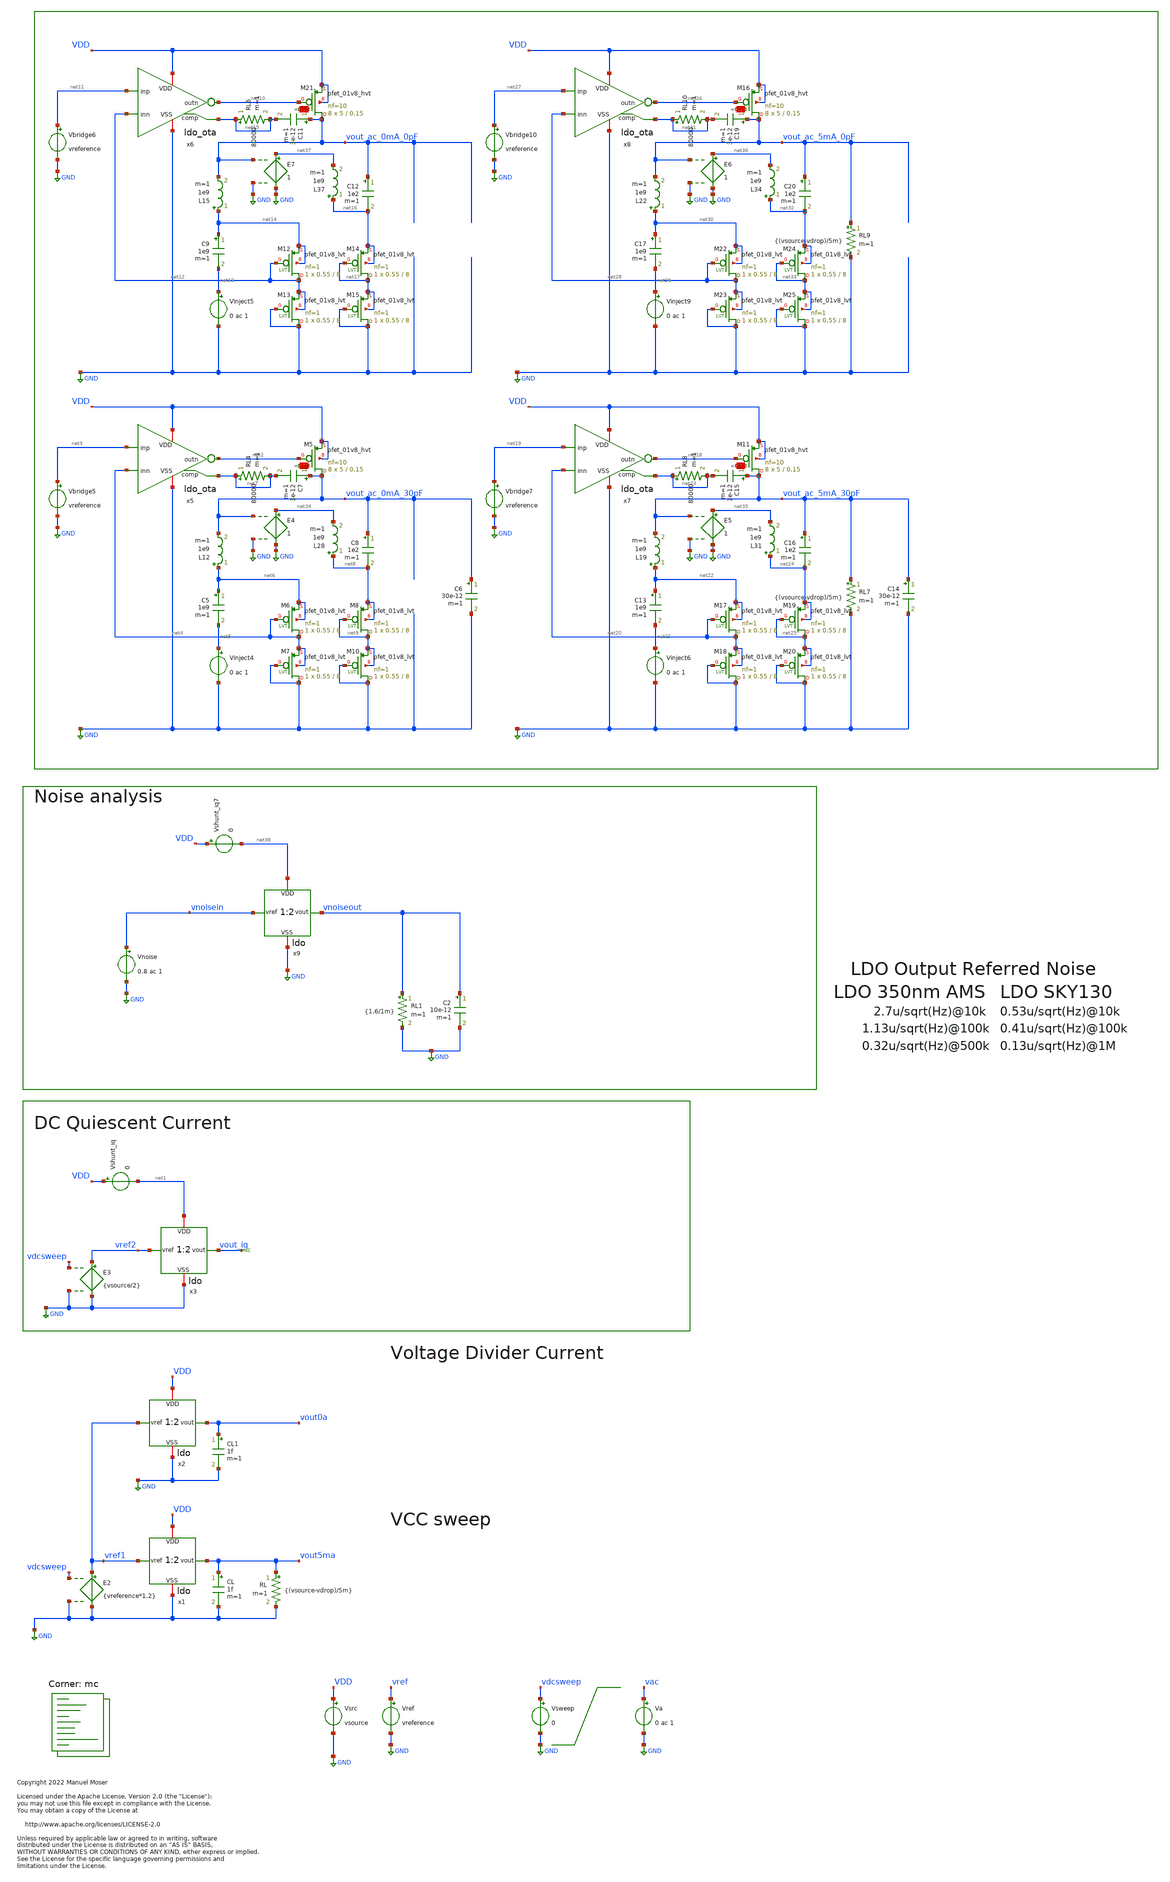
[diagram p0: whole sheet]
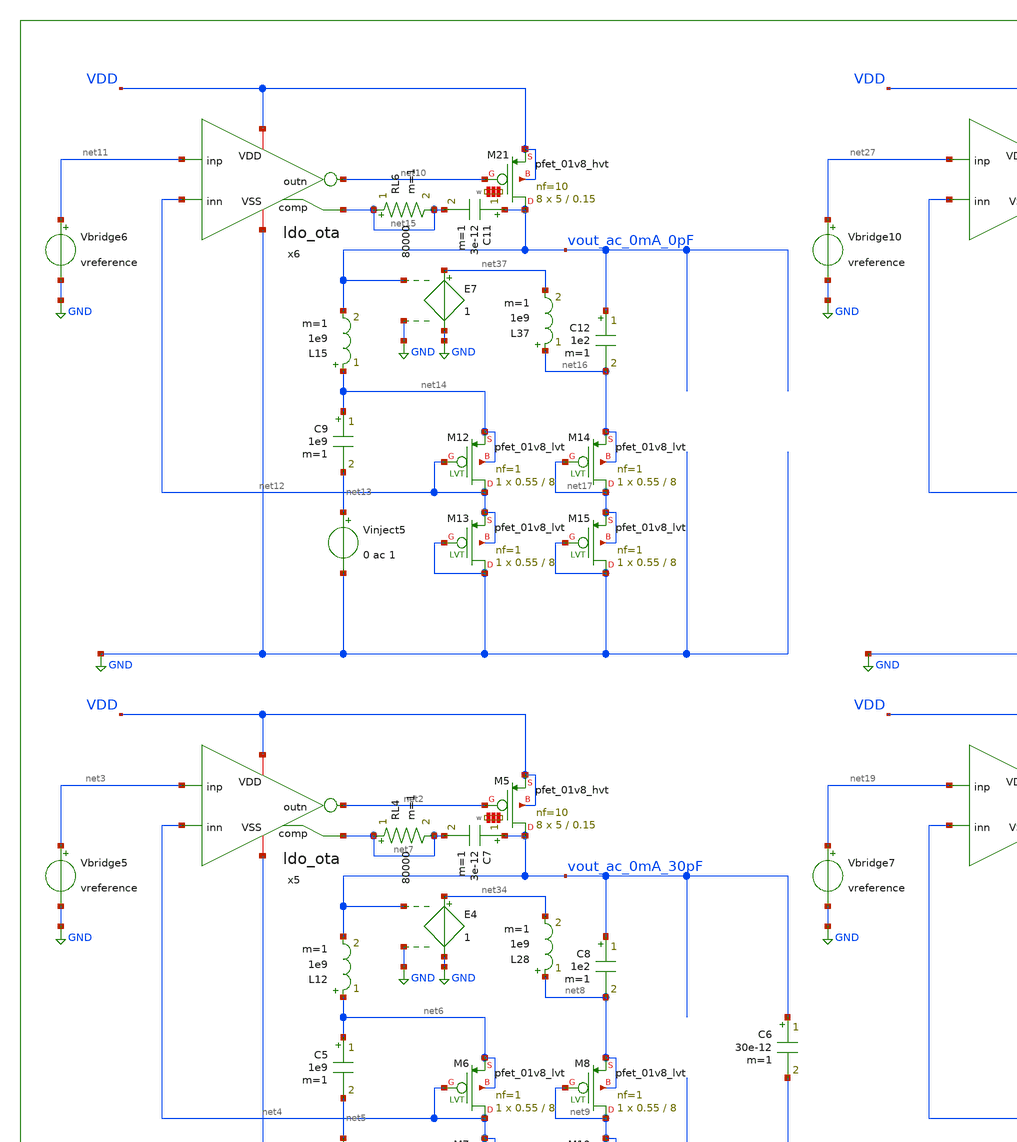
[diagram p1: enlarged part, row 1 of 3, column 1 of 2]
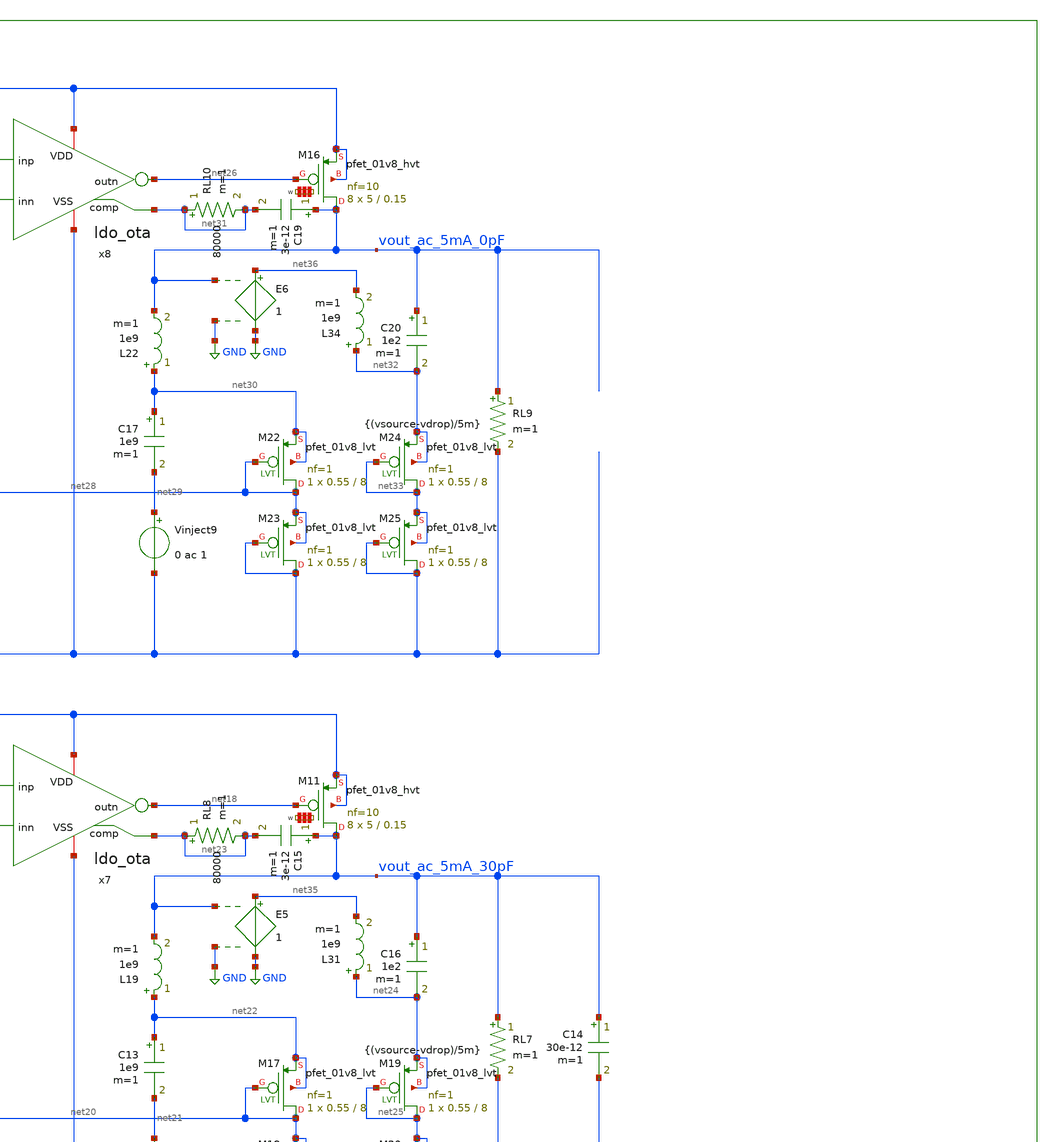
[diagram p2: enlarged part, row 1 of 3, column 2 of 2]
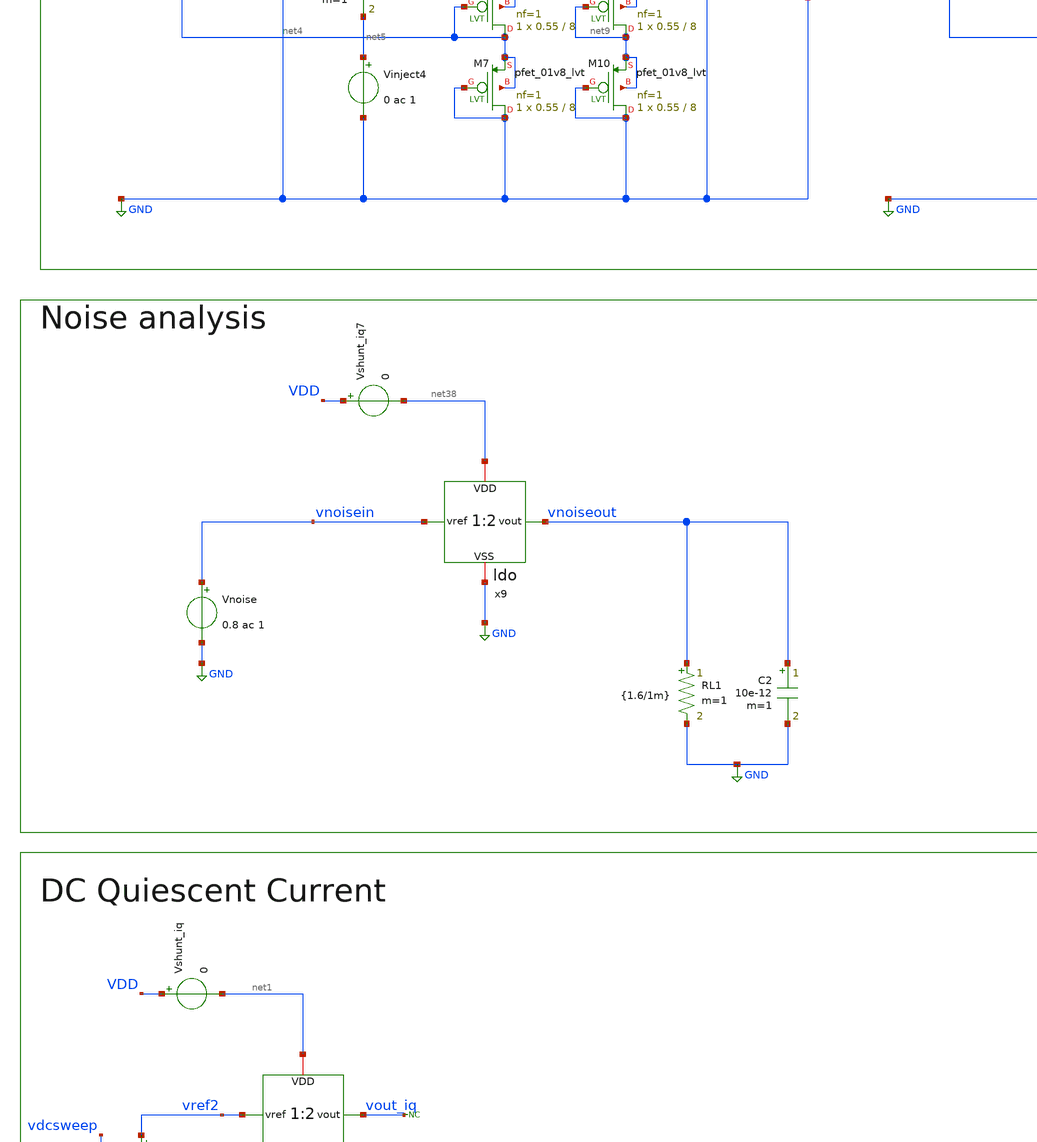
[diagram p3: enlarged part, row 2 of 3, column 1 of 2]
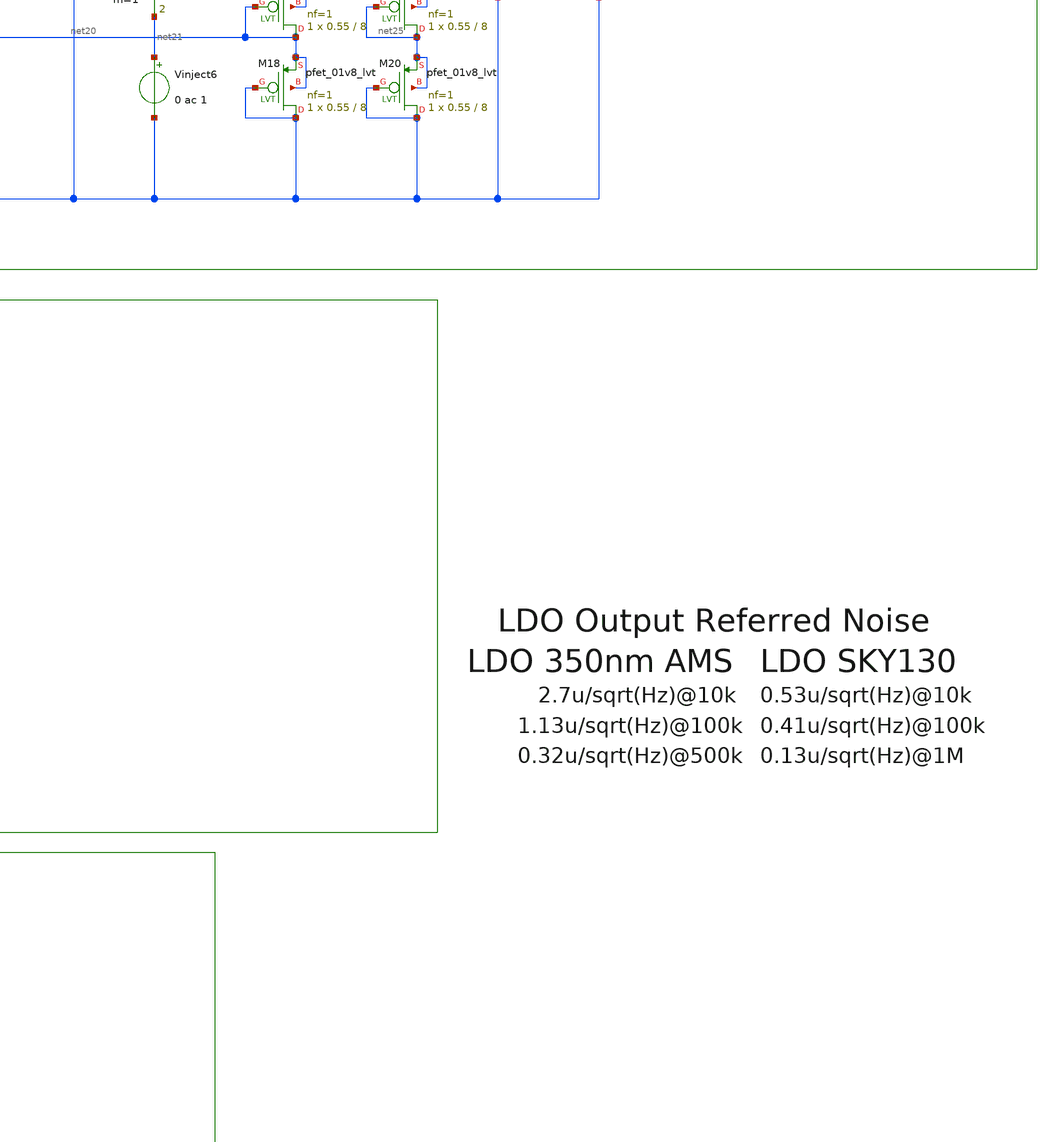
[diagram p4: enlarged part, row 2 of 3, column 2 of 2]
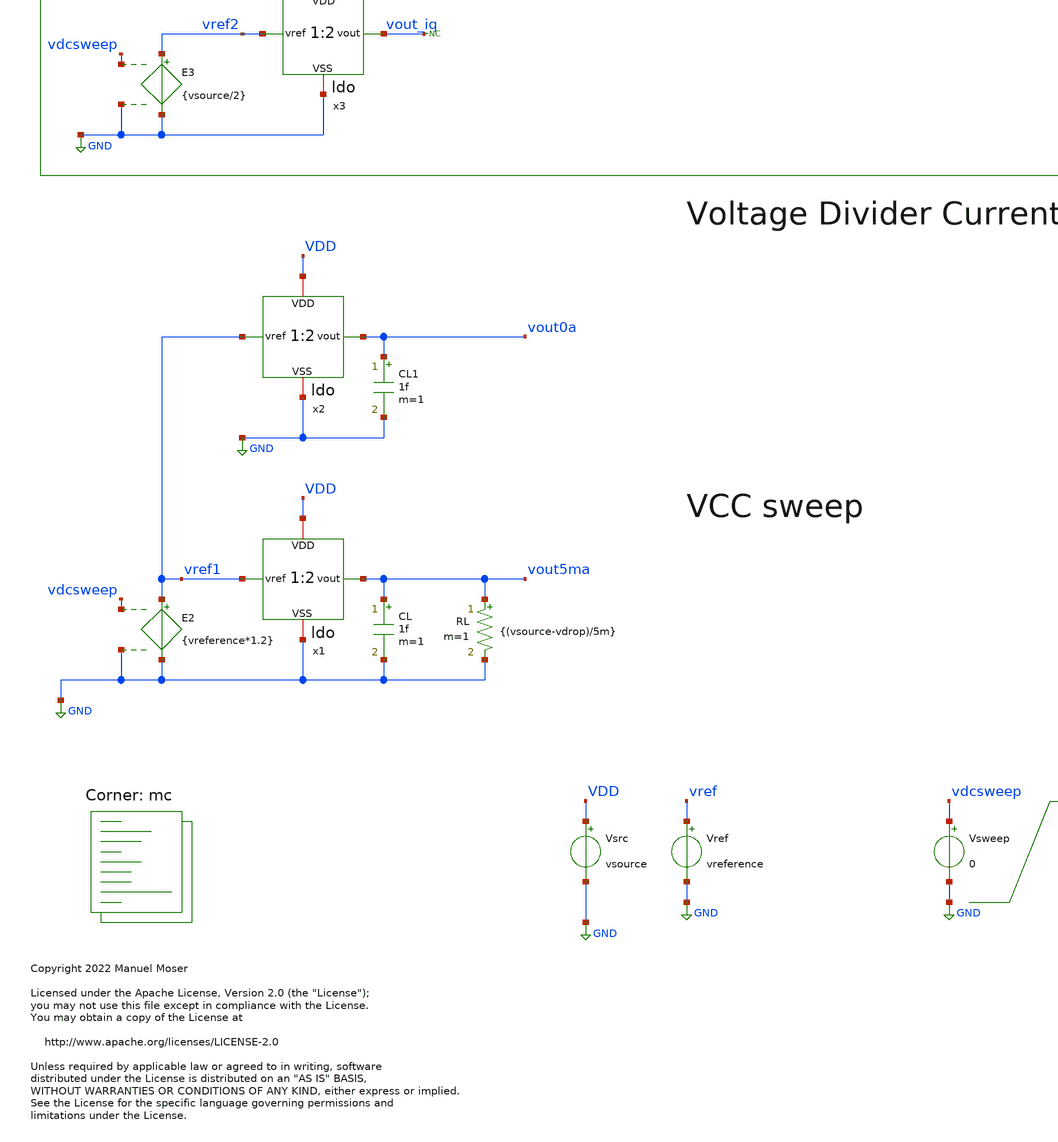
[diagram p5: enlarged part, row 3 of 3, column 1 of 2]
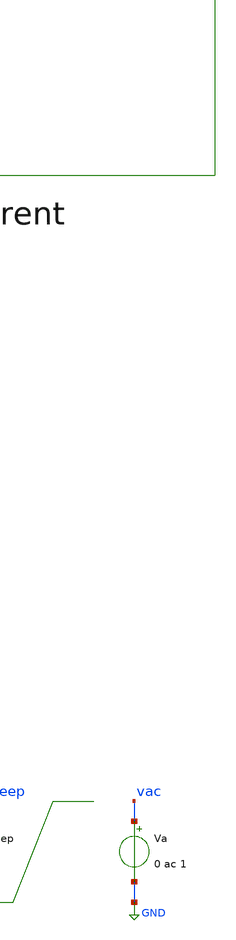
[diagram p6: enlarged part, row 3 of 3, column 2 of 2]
** sch_path: xschem/ldo_tb.sch
* Copyright 2022 Manuel Moser
* Licensed under the Apache License, Version 2.0 (the "License");
**.subckt ldo_tb
Vref vref GND vreference
Vsrc VDD GND vsource
Va vac GND 0 ac 1
CL vout5ma GND 1f m=1
RL vout5ma GND {(vsource-vdrop)/5m} m=1
x1 VDD vref1 vout5ma GND ldo
CL1 vout0a GND 1f m=1
x2 VDD vref1 vout0a GND ldo
Vsweep vdcsweep GND 0
E2 vref1 GND vdcsweep GND {vreference*1.2}
x3 net1 vref2 vout_iq GND ldo
Vshunt_iq VDD net1 0
E3 vref2 GND vdcsweep GND {vsource/2}
* noconn vout_iq
Vnoise vnoisein GND 0.8 ac 1
RL1 vnoiseout GND {1.6/1m} m=1
C2 vnoiseout GND 10e-12 m=1
x5 VDD net3 net2 net4 GND net7 ldo_ota
L12 net6 vout_ac_0mA_30pF 1e9 m=1
C5 net6 net5 1e9 m=1
Vinject4 net5 GND 0 ac 1
Vbridge5 net3 GND vreference
C6 vout_ac_0mA_30pF GND 30e-12 m=1
C7 vout_ac_0mA_30pF net7 3e-12 m=1
RL4 net7 net7 80000 m=1
XM6 net4 net4 net6 net6 sky130_fd_pr__pfet_01v8_lvt L=8 W=0.55 nf=1 ad='int((nf+1)/2) * W/nf * 0.29'
+ as='int((nf+2)/2) * W/nf * 0.29' pd='2*int((nf+1)/2) * (W/nf + 0.29)' ps='2*int((nf+2)/2) * (W/nf + 0.29)'
+ nrd='0.29 / W' nrs='0.29 / W' sa=0 sb=0 sd=0 mult=1 m=1
XM7 GND GND net4 net4 sky130_fd_pr__pfet_01v8_lvt L=8 W=0.55 nf=1 ad='int((nf+1)/2) * W/nf * 0.29' as='int((nf+2)/2) * W/nf * 0.29'
+ pd='2*int((nf+1)/2) * (W/nf + 0.29)' ps='2*int((nf+2)/2) * (W/nf + 0.29)' nrd='0.29 / W' nrs='0.29 / W'
+ sa=0 sb=0 sd=0 mult=1 m=1
XM8 net9 net9 net8 net8 sky130_fd_pr__pfet_01v8_lvt L=8 W=0.55 nf=1 ad='int((nf+1)/2) * W/nf * 0.29'
+ as='int((nf+2)/2) * W/nf * 0.29' pd='2*int((nf+1)/2) * (W/nf + 0.29)' ps='2*int((nf+2)/2) * (W/nf + 0.29)'
+ nrd='0.29 / W' nrs='0.29 / W' sa=0 sb=0 sd=0 mult=1 m=1
XM10 GND GND net9 net9 sky130_fd_pr__pfet_01v8_lvt L=8 W=0.55 nf=1 ad='int((nf+1)/2) * W/nf * 0.29' as='int((nf+2)/2) * W/nf * 0.29'
+ pd='2*int((nf+1)/2) * (W/nf + 0.29)' ps='2*int((nf+2)/2) * (W/nf + 0.29)' nrd='0.29 / W' nrs='0.29 / W'
+ sa=0 sb=0 sd=0 mult=1 m=1
C8 vout_ac_0mA_30pF net8 1e2 m=1
x6 VDD net11 net10 net12 GND net15 ldo_ota
L15 net14 vout_ac_0mA_0pF 1e9 m=1
C9 net14 net13 1e9 m=1
Vinject5 net13 GND 0 ac 1
Vbridge6 net11 GND vreference
C11 vout_ac_0mA_0pF net15 3e-12 m=1
RL6 net15 net15 80000 m=1
XM12 net12 net12 net14 net14 sky130_fd_pr__pfet_01v8_lvt L=8 W=0.55 nf=1 ad='int((nf+1)/2) * W/nf * 0.29'
+ as='int((nf+2)/2) * W/nf * 0.29' pd='2*int((nf+1)/2) * (W/nf + 0.29)' ps='2*int((nf+2)/2) * (W/nf + 0.29)'
+ nrd='0.29 / W' nrs='0.29 / W' sa=0 sb=0 sd=0 mult=1 m=1
XM13 GND GND net12 net12 sky130_fd_pr__pfet_01v8_lvt L=8 W=0.55 nf=1 ad='int((nf+1)/2) * W/nf * 0.29'
+ as='int((nf+2)/2) * W/nf * 0.29' pd='2*int((nf+1)/2) * (W/nf + 0.29)' ps='2*int((nf+2)/2) * (W/nf + 0.29)'
+ nrd='0.29 / W' nrs='0.29 / W' sa=0 sb=0 sd=0 mult=1 m=1
XM14 net17 net17 net16 net16 sky130_fd_pr__pfet_01v8_lvt L=8 W=0.55 nf=1 ad='int((nf+1)/2) * W/nf * 0.29'
+ as='int((nf+2)/2) * W/nf * 0.29' pd='2*int((nf+1)/2) * (W/nf + 0.29)' ps='2*int((nf+2)/2) * (W/nf + 0.29)'
+ nrd='0.29 / W' nrs='0.29 / W' sa=0 sb=0 sd=0 mult=1 m=1
XM15 GND GND net17 net17 sky130_fd_pr__pfet_01v8_lvt L=8 W=0.55 nf=1 ad='int((nf+1)/2) * W/nf * 0.29'
+ as='int((nf+2)/2) * W/nf * 0.29' pd='2*int((nf+1)/2) * (W/nf + 0.29)' ps='2*int((nf+2)/2) * (W/nf + 0.29)'
+ nrd='0.29 / W' nrs='0.29 / W' sa=0 sb=0 sd=0 mult=1 m=1
C12 vout_ac_0mA_0pF net16 1e2 m=1
x7 VDD net19 net18 net20 GND net23 ldo_ota
L19 net22 vout_ac_5mA_30pF 1e9 m=1
C13 net22 net21 1e9 m=1
Vinject6 net21 GND 0 ac 1
Vbridge7 net19 GND vreference
RL7 vout_ac_5mA_30pF GND {(vsource-vdrop)/5m} m=1
C14 vout_ac_5mA_30pF GND 30e-12 m=1
C15 vout_ac_5mA_30pF net23 3e-12 m=1
RL8 net23 net23 80000 m=1
XM17 net20 net20 net22 net22 sky130_fd_pr__pfet_01v8_lvt L=8 W=0.55 nf=1 ad='int((nf+1)/2) * W/nf * 0.29'
+ as='int((nf+2)/2) * W/nf * 0.29' pd='2*int((nf+1)/2) * (W/nf + 0.29)' ps='2*int((nf+2)/2) * (W/nf + 0.29)'
+ nrd='0.29 / W' nrs='0.29 / W' sa=0 sb=0 sd=0 mult=1 m=1
XM18 GND GND net20 net20 sky130_fd_pr__pfet_01v8_lvt L=8 W=0.55 nf=1 ad='int((nf+1)/2) * W/nf * 0.29'
+ as='int((nf+2)/2) * W/nf * 0.29' pd='2*int((nf+1)/2) * (W/nf + 0.29)' ps='2*int((nf+2)/2) * (W/nf + 0.29)'
+ nrd='0.29 / W' nrs='0.29 / W' sa=0 sb=0 sd=0 mult=1 m=1
XM19 net25 net25 net24 net24 sky130_fd_pr__pfet_01v8_lvt L=8 W=0.55 nf=1 ad='int((nf+1)/2) * W/nf * 0.29'
+ as='int((nf+2)/2) * W/nf * 0.29' pd='2*int((nf+1)/2) * (W/nf + 0.29)' ps='2*int((nf+2)/2) * (W/nf + 0.29)'
+ nrd='0.29 / W' nrs='0.29 / W' sa=0 sb=0 sd=0 mult=1 m=1
XM20 GND GND net25 net25 sky130_fd_pr__pfet_01v8_lvt L=8 W=0.55 nf=1 ad='int((nf+1)/2) * W/nf * 0.29'
+ as='int((nf+2)/2) * W/nf * 0.29' pd='2*int((nf+1)/2) * (W/nf + 0.29)' ps='2*int((nf+2)/2) * (W/nf + 0.29)'
+ nrd='0.29 / W' nrs='0.29 / W' sa=0 sb=0 sd=0 mult=1 m=1
C16 vout_ac_5mA_30pF net24 1e2 m=1
x8 VDD net27 net26 net28 GND net31 ldo_ota
L22 net30 vout_ac_5mA_0pF 1e9 m=1
C17 net30 net29 1e9 m=1
Vinject9 net29 GND 0 ac 1
Vbridge10 net27 GND vreference
RL9 vout_ac_5mA_0pF GND {(vsource-vdrop)/5m} m=1
C19 vout_ac_5mA_0pF net31 3e-12 m=1
RL10 net31 net31 80000 m=1
XM22 net28 net28 net30 net30 sky130_fd_pr__pfet_01v8_lvt L=8 W=0.55 nf=1 ad='int((nf+1)/2) * W/nf * 0.29'
+ as='int((nf+2)/2) * W/nf * 0.29' pd='2*int((nf+1)/2) * (W/nf + 0.29)' ps='2*int((nf+2)/2) * (W/nf + 0.29)'
+ nrd='0.29 / W' nrs='0.29 / W' sa=0 sb=0 sd=0 mult=1 m=1
XM23 GND GND net28 net28 sky130_fd_pr__pfet_01v8_lvt L=8 W=0.55 nf=1 ad='int((nf+1)/2) * W/nf * 0.29'
+ as='int((nf+2)/2) * W/nf * 0.29' pd='2*int((nf+1)/2) * (W/nf + 0.29)' ps='2*int((nf+2)/2) * (W/nf + 0.29)'
+ nrd='0.29 / W' nrs='0.29 / W' sa=0 sb=0 sd=0 mult=1 m=1
XM24 net33 net33 net32 net32 sky130_fd_pr__pfet_01v8_lvt L=8 W=0.55 nf=1 ad='int((nf+1)/2) * W/nf * 0.29'
+ as='int((nf+2)/2) * W/nf * 0.29' pd='2*int((nf+1)/2) * (W/nf + 0.29)' ps='2*int((nf+2)/2) * (W/nf + 0.29)'
+ nrd='0.29 / W' nrs='0.29 / W' sa=0 sb=0 sd=0 mult=1 m=1
XM25 GND GND net33 net33 sky130_fd_pr__pfet_01v8_lvt L=8 W=0.55 nf=1 ad='int((nf+1)/2) * W/nf * 0.29'
+ as='int((nf+2)/2) * W/nf * 0.29' pd='2*int((nf+1)/2) * (W/nf + 0.29)' ps='2*int((nf+2)/2) * (W/nf + 0.29)'
+ nrd='0.29 / W' nrs='0.29 / W' sa=0 sb=0 sd=0 mult=1 m=1
C20 vout_ac_5mA_0pF net32 1e2 m=1
L28 net8 net34 1e9 m=1
E4 net34 GND vout_ac_0mA_30pF GND 1
L31 net24 net35 1e9 m=1
E5 net35 GND vout_ac_5mA_30pF GND 1
L34 net32 net36 1e9 m=1
E6 net36 GND vout_ac_5mA_0pF GND 1
L37 net16 net37 1e9 m=1
E7 net37 GND vout_ac_0mA_0pF GND 1
XM5 vout_ac_0mA_30pF net2 VDD VDD sky130_fd_pr__pfet_01v8_hvt L=0.15 W='5 * 10 ' nf=10 ad='int((nf+1)/2) * W / nf * 0.29'
+ as='int((nf+2)/2) * W / nf * 0.29' pd='2*int((nf+1)/2) * (W / nf + 0.29)' ps='2*int((nf+2)/2) * (W / nf + 0.29)'
+ nrd='0.29 / W ' nrs='0.29 / W ' sa=0 sb=0 sd=0 mult=8 m=8
XM11 vout_ac_5mA_30pF net18 VDD VDD sky130_fd_pr__pfet_01v8_hvt L=0.15 W='5 * 10 ' nf=10 ad='int((nf+1)/2) * W / nf * 0.29'
+ as='int((nf+2)/2) * W / nf * 0.29' pd='2*int((nf+1)/2) * (W / nf + 0.29)' ps='2*int((nf+2)/2) * (W / nf + 0.29)'
+ nrd='0.29 / W ' nrs='0.29 / W ' sa=0 sb=0 sd=0 mult=8 m=8
XM16 vout_ac_5mA_0pF net26 VDD VDD sky130_fd_pr__pfet_01v8_hvt L=0.15 W='5 * 10 ' nf=10 ad='int((nf+1)/2) * W / nf * 0.29'
+ as='int((nf+2)/2) * W / nf * 0.29' pd='2*int((nf+1)/2) * (W / nf + 0.29)' ps='2*int((nf+2)/2) * (W / nf + 0.29)'
+ nrd='0.29 / W ' nrs='0.29 / W ' sa=0 sb=0 sd=0 mult=8 m=8
XM21 vout_ac_0mA_0pF net10 VDD VDD sky130_fd_pr__pfet_01v8_hvt L=0.15 W='5 * 10 ' nf=10 ad='int((nf+1)/2) * W / nf * 0.29'
+ as='int((nf+2)/2) * W / nf * 0.29' pd='2*int((nf+1)/2) * (W / nf + 0.29)' ps='2*int((nf+2)/2) * (W / nf + 0.29)'
+ nrd='0.29 / W ' nrs='0.29 / W ' sa=0 sb=0 sd=0 mult=8 m=8
x9 net38 vnoisein vnoiseout GND ldo
Vshunt_iq7 VDD net38 0
**** begin user architecture code



.temp 27
*.option gmin = 1e-16
.option RSHUNT=1E15
.option method = gear

.param vsource = 1.80
.param vdrop = 0.20
.param vreference = {(vsource-vdrop)/2}

.save all
.options savecurrents

.control
set num_threads = 12
write results_ldo.raw
set appendwrite

noise v(vnoiseout) Vnoise dec 10 1 100meg
write results_ldo.raw noise1.all noise2.all

repeat 5
reset

dc vsweep 0 1 0.01 temp -30 60 90
write results_ldo.raw   vref1 vout5ma vout0a x1.vota x1.vfb
+ @m.x1.xm9.msky130_fd_pr__pfet_01v8_lvt[id]  vref2 i(vshunt_iq)

ac dec 10 1 10meg
write results_ldo.raw vout_ac_0mA_0pF vout_ac_0mA_30pF vout_ac_5mA_0pF vout_ac_5mA_30pF

*pz vinject gnd vout_ac_gain gnd vol pz


end

.endc




.lib $::SKYWATER_MODELS/sky130.lib.spice mc
**** end user architecture code
**.ends

* expanding   symbol:  ldo.sym # of pins=4
** sym_path: xschem/ldo.sym
** sch_path: xschem/ldo.sch
.subckt ldo VDD vref vout VSS
*.ipin vref
*.iopin VDD
*.iopin VSS
*.opin vout
x1 VDD vref vota vfb VSS net1 ldo_ota
XM1 vout vota VDD VDD sky130_fd_pr__pfet_01v8 L=0.15 W='5 * 5 ' nf=5 ad='int((nf+1)/2) * W / nf * 0.29'
+ as='int((nf+2)/2) * W / nf * 0.29' pd='2*int((nf+1)/2) * (W / nf + 0.29)' ps='2*int((nf+2)/2) * (W / nf + 0.29)'
+ nrd='0.29 / W ' nrs='0.29 / W ' sa=0 sb=0 sd=0 mult=14 m=14
C1 vout net2 3e-12 m=1
RL2 net1 net2 80000 m=1
XM9 vfb vfb vout vout sky130_fd_pr__pfet_01v8_lvt L=8 W=0.55 nf=1 ad='int((nf+1)/2) * W/nf * 0.29' as='int((nf+2)/2) * W/nf * 0.29'
+ pd='2*int((nf+1)/2) * (W/nf + 0.29)' ps='2*int((nf+2)/2) * (W/nf + 0.29)' nrd='0.29 / W' nrs='0.29 / W'
+ sa=0 sb=0 sd=0 mult=1 m=1
XM3 VSS VSS vfb vfb sky130_fd_pr__pfet_01v8_lvt L=8 W=0.55 nf=1 ad='int((nf+1)/2) * W/nf * 0.29' as='int((nf+2)/2) * W/nf * 0.29'
+ pd='2*int((nf+1)/2) * (W/nf + 0.29)' ps='2*int((nf+2)/2) * (W/nf + 0.29)' nrd='0.29 / W' nrs='0.29 / W'
+ sa=0 sb=0 sd=0 mult=1 m=1
.ends


* expanding   symbol:  ldo_ota.sym # of pins=6
** sym_path: xschem/ldo_ota.sym
** sch_path: xschem/ldo_ota.sch
.subckt ldo_ota VDD inp outn inn VSS comp
*.iopin VDD
*.iopin VSS
*.ipin inp
*.ipin inn
*.opin outn
*.opin comp
x2 bias2 VDD VSS bias1 ldo_isource
XM10 net1 bias2 VDD VDD sky130_fd_pr__pfet_01v8_lvt L=8 W='0.55 * 1 ' nf=1 ad='int((nf+1)/2) * W / nf * 0.29'
+ as='int((nf+2)/2) * W / nf * 0.29' pd='2*int((nf+1)/2) * (W / nf + 0.29)' ps='2*int((nf+2)/2) * (W / nf + 0.29)'
+ nrd='0.29 / W ' nrs='0.29 / W ' sa=0 sb=0 sd=0 mult=1 m=1
XM12 bias2 bias2 net1 VDD sky130_fd_pr__pfet_01v8_lvt L=8 W='0.55 * 4 ' nf=4 ad='int((nf+1)/2) * W / nf * 0.29'
+ as='int((nf+2)/2) * W / nf * 0.29' pd='2*int((nf+1)/2) * (W / nf + 0.29)' ps='2*int((nf+2)/2) * (W / nf + 0.29)'
+ nrd='0.29 / W ' nrs='0.29 / W ' sa=0 sb=0 sd=0 mult=1 m=1
XM1 net2 bias1 VDD VDD sky130_fd_pr__pfet_01v8_lvt L=8 W='0.55 * 4 ' nf=4 ad='int((nf+1)/2) * W / nf * 0.29'
+ as='int((nf+2)/2) * W / nf * 0.29' pd='2*int((nf+1)/2) * (W / nf + 0.29)' ps='2*int((nf+2)/2) * (W / nf + 0.29)'
+ nrd='0.29 / W ' nrs='0.29 / W ' sa=0 sb=0 sd=0 mult=1 m=1
XM2 bias1 bias2 net2 VDD sky130_fd_pr__pfet_01v8_lvt L=8 W='0.55 * 4 ' nf=4 ad='int((nf+1)/2) * W / nf * 0.29'
+ as='int((nf+2)/2) * W / nf * 0.29' pd='2*int((nf+1)/2) * (W / nf + 0.29)' ps='2*int((nf+2)/2) * (W / nf + 0.29)'
+ nrd='0.29 / W ' nrs='0.29 / W ' sa=0 sb=0 sd=0 mult=1 m=1
XM3 net3 bias1 VDD VDD sky130_fd_pr__pfet_01v8_lvt L=8 W='0.55 * 4 ' nf=4 ad='int((nf+1)/2) * W / nf * 0.29'
+ as='int((nf+2)/2) * W / nf * 0.29' pd='2*int((nf+1)/2) * (W / nf + 0.29)' ps='2*int((nf+2)/2) * (W / nf + 0.29)'
+ nrd='0.29 / W ' nrs='0.29 / W ' sa=0 sb=0 sd=0 mult=1 m=1
XM4 bias3 bias2 net3 VDD sky130_fd_pr__pfet_01v8_lvt L=8 W='0.55 * 4 ' nf=4 ad='int((nf+1)/2) * W / nf * 0.29'
+ as='int((nf+2)/2) * W / nf * 0.29' pd='2*int((nf+1)/2) * (W / nf + 0.29)' ps='2*int((nf+2)/2) * (W / nf + 0.29)'
+ nrd='0.29 / W ' nrs='0.29 / W ' sa=0 sb=0 sd=0 mult=1 m=1
XM5 net4 bias1 VDD VDD sky130_fd_pr__pfet_01v8_lvt L=8 W='0.55 * 4 ' nf=4 ad='int((nf+1)/2) * W / nf * 0.29'
+ as='int((nf+2)/2) * W / nf * 0.29' pd='2*int((nf+1)/2) * (W / nf + 0.29)' ps='2*int((nf+2)/2) * (W / nf + 0.29)'
+ nrd='0.29 / W ' nrs='0.29 / W ' sa=0 sb=0 sd=0 mult=1 m=1
XM8 bias4 bias2 net4 VDD sky130_fd_pr__pfet_01v8_lvt L=8 W='0.55 * 4 ' nf=4 ad='int((nf+1)/2) * W / nf * 0.29'
+ as='int((nf+2)/2) * W / nf * 0.29' pd='2*int((nf+1)/2) * (W / nf + 0.29)' ps='2*int((nf+2)/2) * (W / nf + 0.29)'
+ nrd='0.29 / W ' nrs='0.29 / W ' sa=0 sb=0 sd=0 mult=1 m=1
XM9 bias3 bias3 net5 VSS sky130_fd_pr__nfet_01v8_lvt L=4 W='1 * 2 ' nf=2 ad='int((nf+1)/2) * W / nf * 0.29'
+ as='int((nf+2)/2) * W / nf * 0.29' pd='2*int((nf+1)/2) * (W / nf + 0.29)' ps='2*int((nf+2)/2) * (W / nf + 0.29)'
+ nrd='0.29 / W ' nrs='0.29 / W ' sa=0 sb=0 sd=0 mult=1 m=1
XM11 net5 bias3 net10 VSS sky130_fd_pr__nfet_01v8 L=8 W='0.42 * 1 ' nf=1 ad='int((nf+1)/2) * W / nf * 0.29'
+ as='int((nf+2)/2) * W / nf * 0.29' pd='2*int((nf+1)/2) * (W / nf + 0.29)' ps='2*int((nf+2)/2) * (W / nf + 0.29)'
+ nrd='0.29 / W ' nrs='0.29 / W ' sa=0 sb=0 sd=0 mult=1 m=1
XM13 bias4 bias3 net6 VSS sky130_fd_pr__nfet_01v8_lvt L=4 W='1 * 2 ' nf=2 ad='int((nf+1)/2) * W / nf * 0.29'
+ as='int((nf+2)/2) * W / nf * 0.29' pd='2*int((nf+1)/2) * (W / nf + 0.29)' ps='2*int((nf+2)/2) * (W / nf + 0.29)'
+ nrd='0.29 / W ' nrs='0.29 / W ' sa=0 sb=0 sd=0 mult=1 m=1
XM14 net6 bias4 net7 VSS sky130_fd_pr__nfet_01v8 L=8 W='0.42 * 4 ' nf=4 ad='int((nf+1)/2) * W / nf * 0.29'
+ as='int((nf+2)/2) * W / nf * 0.29' pd='2*int((nf+1)/2) * (W / nf + 0.29)' ps='2*int((nf+2)/2) * (W / nf + 0.29)'
+ nrd='0.29 / W ' nrs='0.29 / W ' sa=0 sb=0 sd=0 mult=1 m=1
XM6 net7 bias4 net8 VSS sky130_fd_pr__nfet_01v8 L=8 W='0.42 * 4 ' nf=4 ad='int((nf+1)/2) * W / nf * 0.29'
+ as='int((nf+2)/2) * W / nf * 0.29' pd='2*int((nf+1)/2) * (W / nf + 0.29)' ps='2*int((nf+2)/2) * (W / nf + 0.29)'
+ nrd='0.29 / W ' nrs='0.29 / W ' sa=0 sb=0 sd=0 mult=1 m=1
XM7 net10 bias3 net9 VSS sky130_fd_pr__nfet_01v8 L=8 W='0.42 * 1 ' nf=1 ad='int((nf+1)/2) * W / nf * 0.29'
+ as='int((nf+2)/2) * W / nf * 0.29' pd='2*int((nf+1)/2) * (W / nf + 0.29)' ps='2*int((nf+2)/2) * (W / nf + 0.29)'
+ nrd='0.29 / W ' nrs='0.29 / W ' sa=0 sb=0 sd=0 mult=1 m=1
x1 VDD inp inn bias1 bias2 bias3 outn VSS bias4 comp ldo_fc_n
XM15 net9 bias3 net11 VSS sky130_fd_pr__nfet_01v8 L=8 W='0.42 * 1 ' nf=1 ad='int((nf+1)/2) * W / nf * 0.29'
+ as='int((nf+2)/2) * W / nf * 0.29' pd='2*int((nf+1)/2) * (W / nf + 0.29)' ps='2*int((nf+2)/2) * (W / nf + 0.29)'
+ nrd='0.29 / W ' nrs='0.29 / W ' sa=0 sb=0 sd=0 mult=1 m=1
XM16 net8 bias4 net12 VSS sky130_fd_pr__nfet_01v8 L=8 W='0.42 * 4 ' nf=4 ad='int((nf+1)/2) * W / nf * 0.29'
+ as='int((nf+2)/2) * W / nf * 0.29' pd='2*int((nf+1)/2) * (W / nf + 0.29)' ps='2*int((nf+2)/2) * (W / nf + 0.29)'
+ nrd='0.29 / W ' nrs='0.29 / W ' sa=0 sb=0 sd=0 mult=1 m=1
XM17 net12 bias4 VSS VSS sky130_fd_pr__nfet_01v8 L=8 W='0.42 * 4 ' nf=4 ad='int((nf+1)/2) * W / nf * 0.29'
+ as='int((nf+2)/2) * W / nf * 0.29' pd='2*int((nf+1)/2) * (W / nf + 0.29)' ps='2*int((nf+2)/2) * (W / nf + 0.29)'
+ nrd='0.29 / W ' nrs='0.29 / W ' sa=0 sb=0 sd=0 mult=1 m=1
XM18 net11 bias3 VSS VSS sky130_fd_pr__nfet_01v8 L=8 W='0.42 * 1 ' nf=1 ad='int((nf+1)/2) * W / nf * 0.29'
+ as='int((nf+2)/2) * W / nf * 0.29' pd='2*int((nf+1)/2) * (W / nf + 0.29)' ps='2*int((nf+2)/2) * (W / nf + 0.29)'
+ nrd='0.29 / W ' nrs='0.29 / W ' sa=0 sb=0 sd=0 mult=1 m=1
.ends


* expanding   symbol:  ldo_isource.sym # of pins=4
** sym_path: xschem/ldo_isource.sym
** sch_path: xschem/ldo_isource.sch
.subckt ldo_isource curr_n1 VDD VSS curr_n2
*.iopin VDD
*.iopin VSS
*.ipin curr_n1
*.ipin curr_n2
XMP2 VGP VGP net4 VDD sky130_fd_pr__pfet_01v8_lvt L=8 W='0.55 * 7 ' nf=7 ad='int((nf+1)/2) * W / nf * 0.29'
+ as='int((nf+2)/2) * W / nf * 0.29' pd='2*int((nf+1)/2) * (W / nf + 0.29)' ps='2*int((nf+2)/2) * (W / nf + 0.29)'
+ nrd='0.29 / W ' nrs='0.29 / W ' sa=0 sb=0 sd=0 mult=1 m=1
XMP1 VGN VGP net3 VDD sky130_fd_pr__pfet_01v8_lvt L=8 W='0.55 * 7 ' nf=7 ad='int((nf+1)/2) * W / nf * 0.29'
+ as='int((nf+2)/2) * W / nf * 0.29' pd='2*int((nf+1)/2) * (W / nf + 0.29)' ps='2*int((nf+2)/2) * (W / nf + 0.29)'
+ nrd='0.29 / W ' nrs='0.29 / W ' sa=0 sb=0 sd=0 mult=1 m=1
XMN1 VGN VGN net1 VSS sky130_fd_pr__nfet_01v8_lvt L=8 W='7 * 1 ' nf=1 ad='int((nf+1)/2) * W / nf * 0.29'
+ as='int((nf+2)/2) * W / nf * 0.29' pd='2*int((nf+1)/2) * (W / nf + 0.29)' ps='2*int((nf+2)/2) * (W / nf + 0.29)'
+ nrd='0.29 / W ' nrs='0.29 / W ' sa=0 sb=0 sd=0 mult=1 m=1
XMN2 VGP VGN net2 VSS sky130_fd_pr__nfet_01v8_lvt L=8 W='7 * 1 ' nf=1 ad='int((nf+1)/2) * W / nf * 0.29'
+ as='int((nf+2)/2) * W / nf * 0.29' pd='2*int((nf+1)/2) * (W / nf + 0.29)' ps='2*int((nf+2)/2) * (W / nf + 0.29)'
+ nrd='0.29 / W ' nrs='0.29 / W ' sa=0 sb=0 sd=0 mult=5 m=5
XMN3 net1 VGN VSS VSS sky130_fd_pr__nfet_01v8_lvt L=8 W='7 * 1 ' nf=1 ad='int((nf+1)/2) * W / nf * 0.29'
+ as='int((nf+2)/2) * W / nf * 0.29' pd='2*int((nf+1)/2) * (W / nf + 0.29)' ps='2*int((nf+2)/2) * (W / nf + 0.29)'
+ nrd='0.29 / W ' nrs='0.29 / W ' sa=0 sb=0 sd=0 mult=1 m=1
XMN4 net2 VGN Vref VSS sky130_fd_pr__nfet_01v8_lvt L=8 W='7 * 1 ' nf=1 ad='int((nf+1)/2) * W / nf * 0.29'
+ as='int((nf+2)/2) * W / nf * 0.29' pd='2*int((nf+1)/2) * (W / nf + 0.29)' ps='2*int((nf+2)/2) * (W / nf + 0.29)'
+ nrd='0.29 / W ' nrs='0.29 / W ' sa=0 sb=0 sd=0 mult=5 m=5
XMP4 net3 VGP VDD VDD sky130_fd_pr__pfet_01v8_lvt L=8 W='0.55 * 7 ' nf=7 ad='int((nf+1)/2) * W / nf * 0.29'
+ as='int((nf+2)/2) * W / nf * 0.29' pd='2*int((nf+1)/2) * (W / nf + 0.29)' ps='2*int((nf+2)/2) * (W / nf + 0.29)'
+ nrd='0.29 / W ' nrs='0.29 / W ' sa=0 sb=0 sd=0 mult=1 m=1
XMP5 net4 VGP VDD VDD sky130_fd_pr__pfet_01v8_lvt L=8 W='0.55 * 7 ' nf=7 ad='int((nf+1)/2) * W / nf * 0.29'
+ as='int((nf+2)/2) * W / nf * 0.29' pd='2*int((nf+1)/2) * (W / nf + 0.29)' ps='2*int((nf+2)/2) * (W / nf + 0.29)'
+ nrd='0.29 / W ' nrs='0.29 / W ' sa=0 sb=0 sd=0 mult=1 m=1
XMP3 Vrefgate VGP net19 VDD sky130_fd_pr__pfet_01v8_lvt L=8 W='0.55 * 7 ' nf=7 ad='int((nf+1)/2) * W / nf * 0.29'
+ as='int((nf+2)/2) * W / nf * 0.29' pd='2*int((nf+1)/2) * (W / nf + 0.29)' ps='2*int((nf+2)/2) * (W / nf + 0.29)'
+ nrd='0.29 / W ' nrs='0.29 / W ' sa=0 sb=0 sd=0 mult=1 m=1
XM2 net5 Vrefgate net6 VSS sky130_fd_pr__nfet_01v8 L=4 W='1 * 1 ' nf=1 ad='int((nf+1)/2) * W / nf * 0.29'
+ as='int((nf+2)/2) * W / nf * 0.29' pd='2*int((nf+1)/2) * (W / nf + 0.29)' ps='2*int((nf+2)/2) * (W / nf + 0.29)'
+ nrd='0.29 / W ' nrs='0.29 / W ' sa=0 sb=0 sd=0 mult=1 m=1
XM3 net8 Vrefgate VSS VSS sky130_fd_pr__nfet_01v8 L=4 W='1 * 1 ' nf=1 ad='int((nf+1)/2) * W / nf * 0.29'
+ as='int((nf+2)/2) * W / nf * 0.29' pd='2*int((nf+1)/2) * (W / nf + 0.29)' ps='2*int((nf+2)/2) * (W / nf + 0.29)'
+ nrd='0.29 / W ' nrs='0.29 / W ' sa=0 sb=0 sd=0 mult=1 m=1
XM1 net7 Vrefgate net8 VSS sky130_fd_pr__nfet_01v8 L=4 W='1 * 1 ' nf=1 ad='int((nf+1)/2) * W / nf * 0.29'
+ as='int((nf+2)/2) * W / nf * 0.29' pd='2*int((nf+1)/2) * (W / nf + 0.29)' ps='2*int((nf+2)/2) * (W / nf + 0.29)'
+ nrd='0.29 / W ' nrs='0.29 / W ' sa=0 sb=0 sd=0 mult=1 m=1
XM4 net6 Vrefgate net7 VSS sky130_fd_pr__nfet_01v8 L=4 W='1 * 1 ' nf=1 ad='int((nf+1)/2) * W / nf * 0.29'
+ as='int((nf+2)/2) * W / nf * 0.29' pd='2*int((nf+1)/2) * (W / nf + 0.29)' ps='2*int((nf+2)/2) * (W / nf + 0.29)'
+ nrd='0.29 / W ' nrs='0.29 / W ' sa=0 sb=0 sd=0 mult=1 m=1
XMN5 net10 Vrefgate VSS VSS sky130_fd_pr__nfet_01v8_lvt L=4 W='1 * 1 ' nf=1 ad='int((nf+1)/2) * W / nf * 0.29'
+ as='int((nf+2)/2) * W / nf * 0.29' pd='2*int((nf+1)/2) * (W / nf + 0.29)' ps='2*int((nf+2)/2) * (W / nf + 0.29)'
+ nrd='0.29 / W ' nrs='0.29 / W ' sa=0 sb=0 sd=0 mult=1 m=1
XMN6 net14 Vrefgate net9 VSS sky130_fd_pr__nfet_01v8_lvt L=4 W='1 * 1 ' nf=1 ad='int((nf+1)/2) * W / nf * 0.29'
+ as='int((nf+2)/2) * W / nf * 0.29' pd='2*int((nf+1)/2) * (W / nf + 0.29)' ps='2*int((nf+2)/2) * (W / nf + 0.29)'
+ nrd='0.29 / W ' nrs='0.29 / W ' sa=0 sb=0 sd=0 mult=1 m=1
XMN9 net16 Vrefgate net14 VSS sky130_fd_pr__nfet_01v8_lvt L=4 W='1 * 1 ' nf=1 ad='int((nf+1)/2) * W / nf * 0.29'
+ as='int((nf+2)/2) * W / nf * 0.29' pd='2*int((nf+1)/2) * (W / nf + 0.29)' ps='2*int((nf+2)/2) * (W / nf + 0.29)'
+ nrd='0.29 / W ' nrs='0.29 / W ' sa=0 sb=0 sd=0 mult=1 m=1
XM5 Vrefgate Vrefgate net5 VSS sky130_fd_pr__nfet_01v8 L=4 W='1 * 1 ' nf=1 ad='int((nf+1)/2) * W / nf * 0.29'
+ as='int((nf+2)/2) * W / nf * 0.29' pd='2*int((nf+1)/2) * (W / nf + 0.29)' ps='2*int((nf+2)/2) * (W / nf + 0.29)'
+ nrd='0.29 / W ' nrs='0.29 / W ' sa=0 sb=0 sd=0 mult=1 m=1
XMN10 net11 Vrefgate net10 VSS sky130_fd_pr__nfet_01v8_lvt L=4 W='1 * 1 ' nf=1 ad='int((nf+1)/2) * W / nf * 0.29'
+ as='int((nf+2)/2) * W / nf * 0.29' pd='2*int((nf+1)/2) * (W / nf + 0.29)' ps='2*int((nf+2)/2) * (W / nf + 0.29)'
+ nrd='0.29 / W ' nrs='0.29 / W ' sa=0 sb=0 sd=0 mult=1 m=1
XMN11 net12 Vrefgate net11 VSS sky130_fd_pr__nfet_01v8_lvt L=4 W='1 * 1 ' nf=1 ad='int((nf+1)/2) * W / nf * 0.29'
+ as='int((nf+2)/2) * W / nf * 0.29' pd='2*int((nf+1)/2) * (W / nf + 0.29)' ps='2*int((nf+2)/2) * (W / nf + 0.29)'
+ nrd='0.29 / W ' nrs='0.29 / W ' sa=0 sb=0 sd=0 mult=1 m=1
XMN12 net13 Vrefgate net12 VSS sky130_fd_pr__nfet_01v8_lvt L=4 W='1 * 1 ' nf=1 ad='int((nf+1)/2) * W / nf * 0.29'
+ as='int((nf+2)/2) * W / nf * 0.29' pd='2*int((nf+1)/2) * (W / nf + 0.29)' ps='2*int((nf+2)/2) * (W / nf + 0.29)'
+ nrd='0.29 / W ' nrs='0.29 / W ' sa=0 sb=0 sd=0 mult=1 m=1
XMN13 net9 Vrefgate net13 VSS sky130_fd_pr__nfet_01v8_lvt L=4 W='1 * 1 ' nf=1 ad='int((nf+1)/2) * W / nf * 0.29'
+ as='int((nf+2)/2) * W / nf * 0.29' pd='2*int((nf+1)/2) * (W / nf + 0.29)' ps='2*int((nf+2)/2) * (W / nf + 0.29)'
+ nrd='0.29 / W ' nrs='0.29 / W ' sa=0 sb=0 sd=0 mult=1 m=1
XMN7 net18 Vrefgate net15 VSS sky130_fd_pr__nfet_01v8_lvt L=4 W='1 * 1 ' nf=1 ad='int((nf+1)/2) * W / nf * 0.29'
+ as='int((nf+2)/2) * W / nf * 0.29' pd='2*int((nf+1)/2) * (W / nf + 0.29)' ps='2*int((nf+2)/2) * (W / nf + 0.29)'
+ nrd='0.29 / W ' nrs='0.29 / W ' sa=0 sb=0 sd=0 mult=1 m=1
XMN8 Vref Vrefgate net18 VSS sky130_fd_pr__nfet_01v8_lvt L=4 W='1 * 1 ' nf=1 ad='int((nf+1)/2) * W / nf * 0.29'
+ as='int((nf+2)/2) * W / nf * 0.29' pd='2*int((nf+1)/2) * (W / nf + 0.29)' ps='2*int((nf+2)/2) * (W / nf + 0.29)'
+ nrd='0.29 / W ' nrs='0.29 / W ' sa=0 sb=0 sd=0 mult=1 m=1
XMN14 net17 Vrefgate net16 VSS sky130_fd_pr__nfet_01v8_lvt L=4 W='1 * 1 ' nf=1 ad='int((nf+1)/2) * W / nf * 0.29'
+ as='int((nf+2)/2) * W / nf * 0.29' pd='2*int((nf+1)/2) * (W / nf + 0.29)' ps='2*int((nf+2)/2) * (W / nf + 0.29)'
+ nrd='0.29 / W ' nrs='0.29 / W ' sa=0 sb=0 sd=0 mult=1 m=1
XMN15 net15 Vrefgate net17 VSS sky130_fd_pr__nfet_01v8_lvt L=4 W='1 * 1 ' nf=1 ad='int((nf+1)/2) * W / nf * 0.29'
+ as='int((nf+2)/2) * W / nf * 0.29' pd='2*int((nf+1)/2) * (W / nf + 0.29)' ps='2*int((nf+2)/2) * (W / nf + 0.29)'
+ nrd='0.29 / W ' nrs='0.29 / W ' sa=0 sb=0 sd=0 mult=1 m=1
XMP6 net19 VGP VDD VDD sky130_fd_pr__pfet_01v8_lvt L=8 W='0.55 * 7 ' nf=7 ad='int((nf+1)/2) * W / nf * 0.29'
+ as='int((nf+2)/2) * W / nf * 0.29' pd='2*int((nf+1)/2) * (W / nf + 0.29)' ps='2*int((nf+2)/2) * (W / nf + 0.29)'
+ nrd='0.29 / W ' nrs='0.29 / W ' sa=0 sb=0 sd=0 mult=1 m=1
XMN16 curr_n1 VGN net20 VSS sky130_fd_pr__nfet_01v8_lvt L=8 W='7 * 1 ' nf=1 ad='int((nf+1)/2) * W / nf * 0.29'
+ as='int((nf+2)/2) * W / nf * 0.29' pd='2*int((nf+1)/2) * (W / nf + 0.29)' ps='2*int((nf+2)/2) * (W / nf + 0.29)'
+ nrd='0.29 / W ' nrs='0.29 / W ' sa=0 sb=0 sd=0 mult=1 m=1
XMN17 net20 VGN VSS VSS sky130_fd_pr__nfet_01v8_lvt L=8 W='7 * 1 ' nf=1 ad='int((nf+1)/2) * W / nf * 0.29'
+ as='int((nf+2)/2) * W / nf * 0.29' pd='2*int((nf+1)/2) * (W / nf + 0.29)' ps='2*int((nf+2)/2) * (W / nf + 0.29)'
+ nrd='0.29 / W ' nrs='0.29 / W ' sa=0 sb=0 sd=0 mult=1 m=1
XM6 VGP vstartup VGN VSS sky130_fd_pr__nfet_01v8 L=4 W='1 * 1 ' nf=1 ad='int((nf+1)/2) * W / nf * 0.29'
+ as='int((nf+2)/2) * W / nf * 0.29' pd='2*int((nf+1)/2) * (W / nf + 0.29)' ps='2*int((nf+2)/2) * (W / nf + 0.29)'
+ nrd='0.29 / W ' nrs='0.29 / W ' sa=0 sb=0 sd=0 mult=1 m=1
XM7 vstartup Vrefgate VSS VSS sky130_fd_pr__nfet_01v8 L=4 W='1 * 1 ' nf=1 ad='int((nf+1)/2) * W / nf * 0.29'
+ as='int((nf+2)/2) * W / nf * 0.29' pd='2*int((nf+1)/2) * (W / nf + 0.29)' ps='2*int((nf+2)/2) * (W / nf + 0.29)'
+ nrd='0.29 / W ' nrs='0.29 / W ' sa=0 sb=0 sd=0 mult=1 m=1
XMN18 curr_n2 VGN net21 VSS sky130_fd_pr__nfet_01v8_lvt L=8 W='7 * 1 ' nf=1 ad='int((nf+1)/2) * W / nf * 0.29'
+ as='int((nf+2)/2) * W / nf * 0.29' pd='2*int((nf+1)/2) * (W / nf + 0.29)' ps='2*int((nf+2)/2) * (W / nf + 0.29)'
+ nrd='0.29 / W ' nrs='0.29 / W ' sa=0 sb=0 sd=0 mult=1 m=1
XMN19 net21 VGN VSS VSS sky130_fd_pr__nfet_01v8_lvt L=8 W='7 * 1 ' nf=1 ad='int((nf+1)/2) * W / nf * 0.29'
+ as='int((nf+2)/2) * W / nf * 0.29' pd='2*int((nf+1)/2) * (W / nf + 0.29)' ps='2*int((nf+2)/2) * (W / nf + 0.29)'
+ nrd='0.29 / W ' nrs='0.29 / W ' sa=0 sb=0 sd=0 mult=1 m=1
XC1 VDD vstartup sky130_fd_pr__cap_mim_m3_2 W=4 L=4 MF=1 m=1
.ends


* expanding   symbol:  ldo_fc_n.sym # of pins=10
** sym_path: xschem/ldo_fc_n.sym
** sch_path: xschem/ldo_fc_n.sch
.subckt ldo_fc_n VDD inp inn bias1 bias2 bias3 outn VSS bias4 comp
*.iopin VSS
*.iopin VDD
*.ipin inp
*.ipin inn
*.ipin bias1
*.opin outn
*.ipin bias2
*.ipin bias3
*.ipin bias4
*.opin comp
XMN4 outn bias3 net1 VSS sky130_fd_pr__nfet_01v8_lvt L=4 W='1 * 2 ' nf=2 ad='int((nf+1)/2) * W / nf * 0.29'
+ as='int((nf+2)/2) * W / nf * 0.29' pd='2*int((nf+1)/2) * (W / nf + 0.29)' ps='2*int((nf+2)/2) * (W / nf + 0.29)'
+ nrd='0.29 / W ' nrs='0.29 / W ' sa=0 sb=0 sd=0 mult=7 m=7
XMN7 net1 net3 net7 VSS sky130_fd_pr__nfet_01v8 L=8 W='0.42 * 4 ' nf=4 ad='int((nf+1)/2) * W / nf * 0.29'
+ as='int((nf+2)/2) * W / nf * 0.29' pd='2*int((nf+1)/2) * (W / nf + 0.29)' ps='2*int((nf+2)/2) * (W / nf + 0.29)'
+ nrd='0.29 / W ' nrs='0.29 / W ' sa=0 sb=0 sd=0 mult=7 m=7
XMN3 net3 bias3 net2 VSS sky130_fd_pr__nfet_01v8_lvt L=4 W='1 * 2 ' nf=2 ad='int((nf+1)/2) * W / nf * 0.29'
+ as='int((nf+2)/2) * W / nf * 0.29' pd='2*int((nf+1)/2) * (W / nf + 0.29)' ps='2*int((nf+2)/2) * (W / nf + 0.29)'
+ nrd='0.29 / W ' nrs='0.29 / W ' sa=0 sb=0 sd=0 mult=7 m=7
XMN6 net2 net3 net6 VSS sky130_fd_pr__nfet_01v8 L=8 W='0.42 * 4 ' nf=4 ad='int((nf+1)/2) * W / nf * 0.29'
+ as='int((nf+2)/2) * W / nf * 0.29' pd='2*int((nf+1)/2) * (W / nf + 0.29)' ps='2*int((nf+2)/2) * (W / nf + 0.29)'
+ nrd='0.29 / W ' nrs='0.29 / W ' sa=0 sb=0 sd=0 mult=7 m=7
XMP4 outn bias2 comp VDD sky130_fd_pr__pfet_01v8_lvt L=8 W='0.55 * 4 ' nf=4 ad='int((nf+1)/2) * W / nf * 0.29'
+ as='int((nf+2)/2) * W / nf * 0.29' pd='2*int((nf+1)/2) * (W / nf + 0.29)' ps='2*int((nf+2)/2) * (W / nf + 0.29)'
+ nrd='0.29 / W ' nrs='0.29 / W ' sa=0 sb=0 sd=0 mult=7 m=7
XMP2 comp bias1 VDD VDD sky130_fd_pr__pfet_01v8_lvt L=8 W='0.55 * 4 ' nf=4 ad='int((nf+1)/2) * W / nf * 0.29'
+ as='int((nf+2)/2) * W / nf * 0.29' pd='2*int((nf+1)/2) * (W / nf + 0.29)' ps='2*int((nf+2)/2) * (W / nf + 0.29)'
+ nrd='0.29 / W ' nrs='0.29 / W ' sa=0 sb=0 sd=0 mult=11 m=11
XMP3 net3 bias2 net4 VDD sky130_fd_pr__pfet_01v8_lvt L=8 W='0.55 * 4 ' nf=4 ad='int((nf+1)/2) * W / nf * 0.29'
+ as='int((nf+2)/2) * W / nf * 0.29' pd='2*int((nf+1)/2) * (W / nf + 0.29)' ps='2*int((nf+2)/2) * (W / nf + 0.29)'
+ nrd='0.29 / W ' nrs='0.29 / W ' sa=0 sb=0 sd=0 mult=7 m=7
XMP1 net4 bias1 VDD VDD sky130_fd_pr__pfet_01v8_lvt L=8 W='0.55 * 4 ' nf=4 ad='int((nf+1)/2) * W / nf * 0.29'
+ as='int((nf+2)/2) * W / nf * 0.29' pd='2*int((nf+1)/2) * (W / nf + 0.29)' ps='2*int((nf+2)/2) * (W / nf + 0.29)'
+ nrd='0.29 / W ' nrs='0.29 / W ' sa=0 sb=0 sd=0 mult=11 m=11
XMN5 net5 bias4 net8 VSS sky130_fd_pr__nfet_01v8 L=8 W='0.42 * 4 ' nf=4 ad='int((nf+1)/2) * W / nf * 0.29'
+ as='int((nf+2)/2) * W / nf * 0.29' pd='2*int((nf+1)/2) * (W / nf + 0.29)' ps='2*int((nf+2)/2) * (W / nf + 0.29)'
+ nrd='0.29 / W ' nrs='0.29 / W ' sa=0 sb=0 sd=0 mult=8 m=8
XMN1 net4 inn net5 VSS sky130_fd_pr__nfet_01v8_lvt L=4 W='1 * 1 ' nf=1 ad='int((nf+1)/2) * W / nf * 0.29'
+ as='int((nf+2)/2) * W / nf * 0.29' pd='2*int((nf+1)/2) * (W / nf + 0.29)' ps='2*int((nf+2)/2) * (W / nf + 0.29)'
+ nrd='0.29 / W ' nrs='0.29 / W ' sa=0 sb=0 sd=0 mult=1 m=1
XMN2 comp inp net5 VSS sky130_fd_pr__nfet_01v8_lvt L=4 W='1 * 1 ' nf=1 ad='int((nf+1)/2) * W / nf * 0.29'
+ as='int((nf+2)/2) * W / nf * 0.29' pd='2*int((nf+1)/2) * (W / nf + 0.29)' ps='2*int((nf+2)/2) * (W / nf + 0.29)'
+ nrd='0.29 / W ' nrs='0.29 / W ' sa=0 sb=0 sd=0 mult=1 m=1
XMN9 net7 net3 net9 VSS sky130_fd_pr__nfet_01v8 L=8 W='0.42 * 4 ' nf=4 ad='int((nf+1)/2) * W / nf * 0.29'
+ as='int((nf+2)/2) * W / nf * 0.29' pd='2*int((nf+1)/2) * (W / nf + 0.29)' ps='2*int((nf+2)/2) * (W / nf + 0.29)'
+ nrd='0.29 / W ' nrs='0.29 / W ' sa=0 sb=0 sd=0 mult=7 m=7
XMN10 net6 net3 net10 VSS sky130_fd_pr__nfet_01v8 L=8 W='0.42 * 4 ' nf=4 ad='int((nf+1)/2) * W / nf * 0.29'
+ as='int((nf+2)/2) * W / nf * 0.29' pd='2*int((nf+1)/2) * (W / nf + 0.29)' ps='2*int((nf+2)/2) * (W / nf + 0.29)'
+ nrd='0.29 / W ' nrs='0.29 / W ' sa=0 sb=0 sd=0 mult=7 m=7
XMN11 net8 bias4 net11 VSS sky130_fd_pr__nfet_01v8 L=8 W='0.42 * 4 ' nf=4 ad='int((nf+1)/2) * W / nf * 0.29'
+ as='int((nf+2)/2) * W / nf * 0.29' pd='2*int((nf+1)/2) * (W / nf + 0.29)' ps='2*int((nf+2)/2) * (W / nf + 0.29)'
+ nrd='0.29 / W ' nrs='0.29 / W ' sa=0 sb=0 sd=0 mult=8 m=8
XMN8 net9 net3 net12 VSS sky130_fd_pr__nfet_01v8 L=8 W='0.42 * 4 ' nf=4 ad='int((nf+1)/2) * W / nf * 0.29'
+ as='int((nf+2)/2) * W / nf * 0.29' pd='2*int((nf+1)/2) * (W / nf + 0.29)' ps='2*int((nf+2)/2) * (W / nf + 0.29)'
+ nrd='0.29 / W ' nrs='0.29 / W ' sa=0 sb=0 sd=0 mult=7 m=7
XMN12 net10 net3 net14 VSS sky130_fd_pr__nfet_01v8 L=8 W='0.42 * 4 ' nf=4 ad='int((nf+1)/2) * W / nf * 0.29'
+ as='int((nf+2)/2) * W / nf * 0.29' pd='2*int((nf+1)/2) * (W / nf + 0.29)' ps='2*int((nf+2)/2) * (W / nf + 0.29)'
+ nrd='0.29 / W ' nrs='0.29 / W ' sa=0 sb=0 sd=0 mult=7 m=7
XMN13 net11 bias4 net13 VSS sky130_fd_pr__nfet_01v8 L=8 W='0.42 * 4 ' nf=4 ad='int((nf+1)/2) * W / nf * 0.29'
+ as='int((nf+2)/2) * W / nf * 0.29' pd='2*int((nf+1)/2) * (W / nf + 0.29)' ps='2*int((nf+2)/2) * (W / nf + 0.29)'
+ nrd='0.29 / W ' nrs='0.29 / W ' sa=0 sb=0 sd=0 mult=8 m=8
XMN14 net12 net3 VSS VSS sky130_fd_pr__nfet_01v8 L=8 W='0.42 * 4 ' nf=4 ad='int((nf+1)/2) * W / nf * 0.29'
+ as='int((nf+2)/2) * W / nf * 0.29' pd='2*int((nf+1)/2) * (W / nf + 0.29)' ps='2*int((nf+2)/2) * (W / nf + 0.29)'
+ nrd='0.29 / W ' nrs='0.29 / W ' sa=0 sb=0 sd=0 mult=7 m=7
XMN15 net14 net3 VSS VSS sky130_fd_pr__nfet_01v8 L=8 W='0.42 * 4 ' nf=4 ad='int((nf+1)/2) * W / nf * 0.29'
+ as='int((nf+2)/2) * W / nf * 0.29' pd='2*int((nf+1)/2) * (W / nf + 0.29)' ps='2*int((nf+2)/2) * (W / nf + 0.29)'
+ nrd='0.29 / W ' nrs='0.29 / W ' sa=0 sb=0 sd=0 mult=7 m=7
XMN16 net13 bias4 VSS VSS sky130_fd_pr__nfet_01v8 L=8 W='0.42 * 4 ' nf=4 ad='int((nf+1)/2) * W / nf * 0.29'
+ as='int((nf+2)/2) * W / nf * 0.29' pd='2*int((nf+1)/2) * (W / nf + 0.29)' ps='2*int((nf+2)/2) * (W / nf + 0.29)'
+ nrd='0.29 / W ' nrs='0.29 / W ' sa=0 sb=0 sd=0 mult=8 m=8
.ends

.GLOBAL GND
.end
